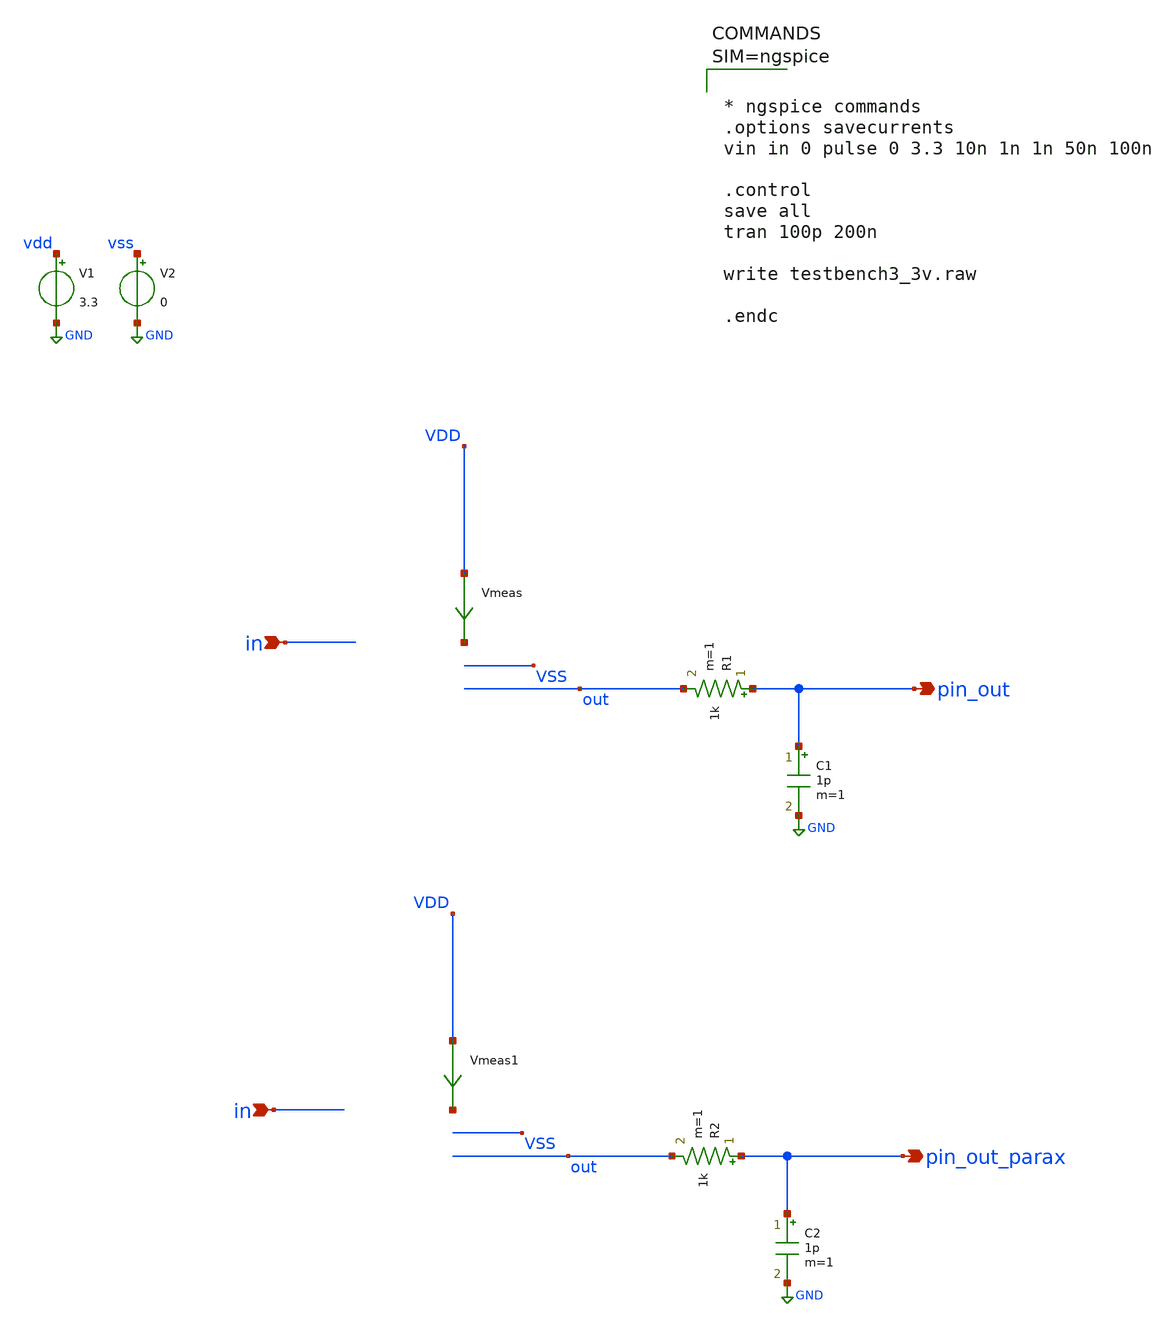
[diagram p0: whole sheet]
** sch_path: tt_um_3v_inverter_SiliconeGuide/xschem/testbench3_3v.sch
**.subckt testbench3_3v pin_out in pin_out_parax in
*.opin pin_out
*.ipin in
*.opin pin_out_parax
*.ipin in
V1 vdd GND 3.3
V2 vss GND 0
R1 pin_out out 1k m=1
C1 pin_out GND 1p m=1
Vmeas VDD net1 0
.save i(vmeas)
R2 pin_out_parax out 1k m=1
C2 pin_out_parax GND 1p m=1
Vmeas1 VDD net2 0
.save i(vmeas1)
**** begin user architecture code



* ngspice commands
.options savecurrents
vin in 0 pulse 0 3.3 10n 1n 1n 50n 100n

.control
save all
tran 100p 200n

write testbench3_3v.raw

.endc






** opencircuitdesign pdks install
.lib $::SKYWATER_MODELS/sky130.lib.spice tt


**** end user architecture code
**.ends
.GLOBAL GND
.end
